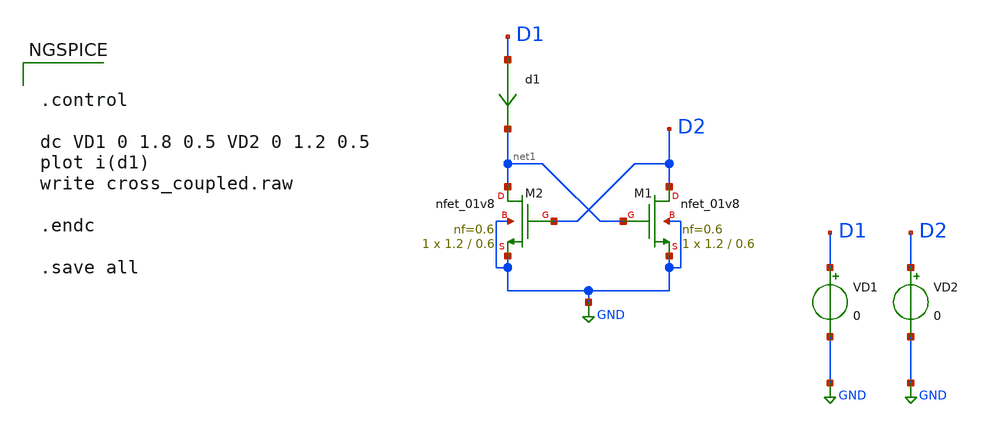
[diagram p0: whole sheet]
** sch_path: cross-couple.sch
**.subckt cross-couple
XM1 D2 net1 GND GND sky130_fd_pr__nfet_01v8 L=0.6 W=1.2 nf=0.6 ad='int((nf+1)/2) * W/nf * 0.29' as='int((nf+2)/2) * W/nf * 0.29'
+ pd='2*int((nf+1)/2) * (W/nf + 0.29)' ps='2*int((nf+2)/2) * (W/nf + 0.29)' nrd='0.29 / W' nrs='0.29 / W'
+ sa=0 sb=0 sd=0 mult=1 m=1
XM2 net1 D2 GND GND sky130_fd_pr__nfet_01v8 L=0.6 W=1.2 nf=0.6 ad='int((nf+1)/2) * W/nf * 0.29' as='int((nf+2)/2) * W/nf * 0.29'
+ pd='2*int((nf+1)/2) * (W/nf + 0.29)' ps='2*int((nf+2)/2) * (W/nf + 0.29)' nrd='0.29 / W' nrs='0.29 / W'
+ sa=0 sb=0 sd=0 mult=1 m=1
VD1 D1 GND 0
VD2 D2 GND 0
d1 D1 net1 0
.save i(d1)
**** begin user architecture code


.control

dc VD1 0 1.8 0.5 VD2 0 1.2 0.5
plot i(d1)
write cross_coupled.raw

.endc

.save all



** opencircuitdesign pdks install
.lib $::SKYWATER_MODELS/sky130.lib.spice tt


**** end user architecture code
**.ends
.GLOBAL GND
.end
